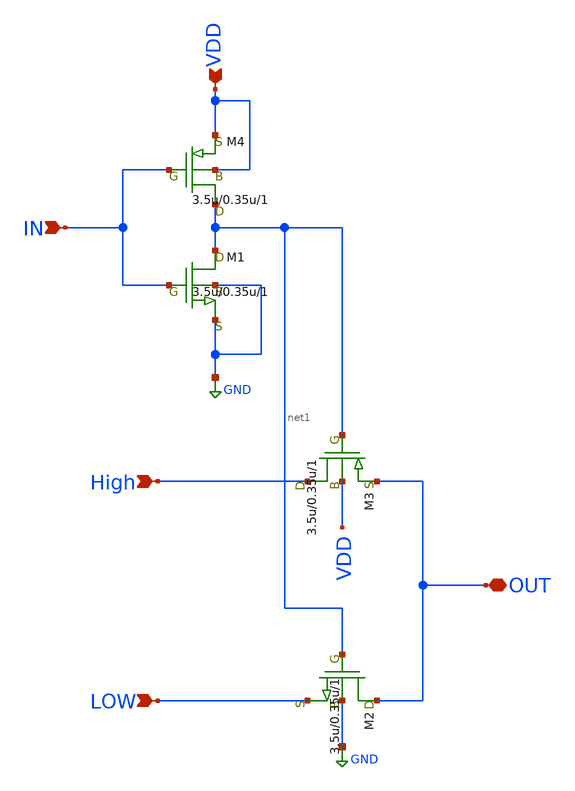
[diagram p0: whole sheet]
** sch_path: LR_Work4/work_1029/SEL.sch
**.subckt SEL High LOW IN VDD OUT
*.ipin High
*.ipin LOW
*.ipin IN
*.ipin VDD
*.iopin OUT
M4 net1 IN VDD VDD p3.0 w=3.5u l=0.35u as=0 ps=0 ad=0 pd=0 m=1
M1 net1 IN GND GND n3.0 w=3.5u l=0.35u as=0 ps=0 ad=0 pd=0 m=1
M2 OUT net1 LOW GND n3.0 w=3.5u l=0.35u as=0 ps=0 ad=0 pd=0 m=1
M3 High net1 OUT VDD p3.0 w=3.5u l=0.35u as=0 ps=0 ad=0 pd=0 m=1
**.ends
.GLOBAL GND
.end
